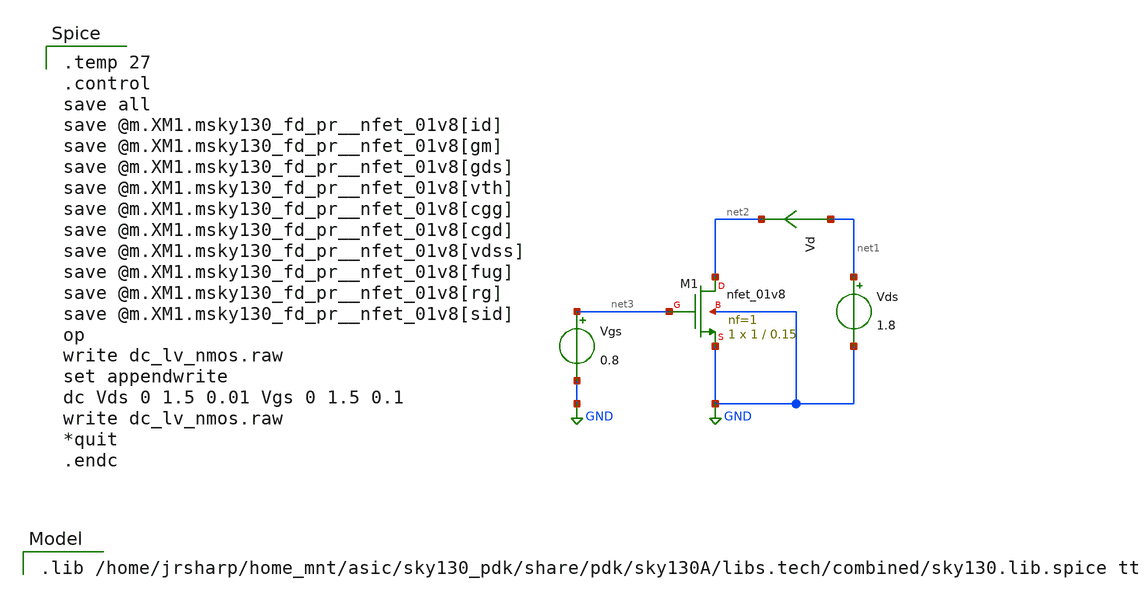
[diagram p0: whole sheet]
** sch_path: 2_1_1-Large-signal-MOSFET-Model/nmos-sweep.sch
**.subckt nmos-sweep
XM1 net2 net3 GND GND sky130_fd_pr__nfet_01v8 L=0.15 W=1 nf=1 ad='int((nf+1)/2) * W/nf * 0.29' as='int((nf+2)/2) * W/nf * 0.29'
+ pd='2*int((nf+1)/2) * (W/nf + 0.29)' ps='2*int((nf+2)/2) * (W/nf + 0.29)' nrd='0.29 / W' nrs='0.29 / W'
+ sa=0 sb=0 sd=0 mult=1 m=1
Vds net1 GND 1.8
Vd net1 net2 0
.save i(vd)
Vgs net3 GND 0.8
**** begin user architecture code

.lib /home/jrsharp/home_mnt/asic/sky130_pdk/share/pdk/sky130A/libs.tech/combined/sky130.lib.spice tt


.temp 27
.control
save all
save @m.XM1.msky130_fd_pr__nfet_01v8[id]
save @m.XM1.msky130_fd_pr__nfet_01v8[gm]
save @m.XM1.msky130_fd_pr__nfet_01v8[gds]
save @m.XM1.msky130_fd_pr__nfet_01v8[vth]
save @m.XM1.msky130_fd_pr__nfet_01v8[cgg]
save @m.XM1.msky130_fd_pr__nfet_01v8[cgd]
save @m.XM1.msky130_fd_pr__nfet_01v8[vdss]
save @m.XM1.msky130_fd_pr__nfet_01v8[fug]
save @m.XM1.msky130_fd_pr__nfet_01v8[rg]
save @m.XM1.msky130_fd_pr__nfet_01v8[sid]
op
write dc_lv_nmos.raw
set appendwrite
dc Vds 0 1.5 0.01 Vgs 0 1.5 0.1
write dc_lv_nmos.raw
*quit
.endc

**** end user architecture code
**.ends
.GLOBAL GND
.end
